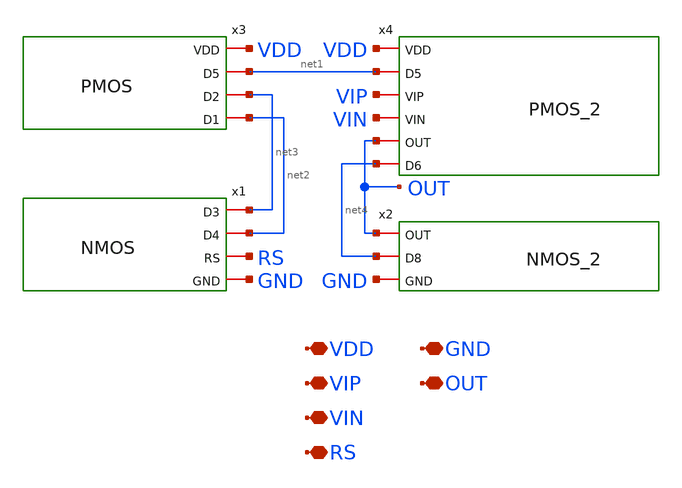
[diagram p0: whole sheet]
** sch_path: OpAmp.sch
**.subckt OpAmp VDD VIP VIN RS GND OUT
*.iopin VDD
*.iopin VIP
*.iopin VIN
*.iopin RS
*.iopin GND
*.iopin OUT
x1 net3 net2 RS GND NMOS
x2 OUT net4 GND NMOS_2
x3 VDD net1 net3 net2 PMOS
x4 VDD net1 VIP VIN OUT net4 PMOS_2
**.ends
.end
